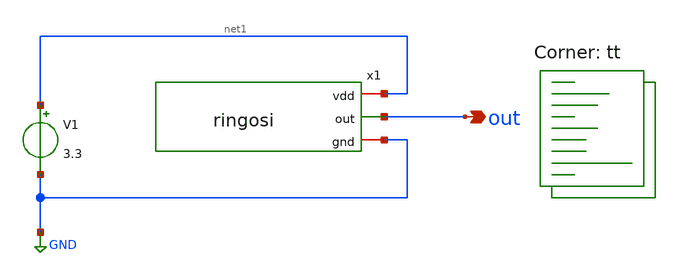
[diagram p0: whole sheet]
** sch_path: ringosi/tbringosi.sch
**.subckt tbringosi out
*.opin out
V1 net1 GND 3.3
x1 net1 out GND ringosi
**** begin user architecture code


.option wnflag=0
.option savecurrents
.control
save all
tran 1ps 10ns
plot out
op
.endc


.lib $::SKYWATER_MODELS/sky130.lib.spice tt
**** end user architecture code
**.ends
.GLOBAL GND
.end
